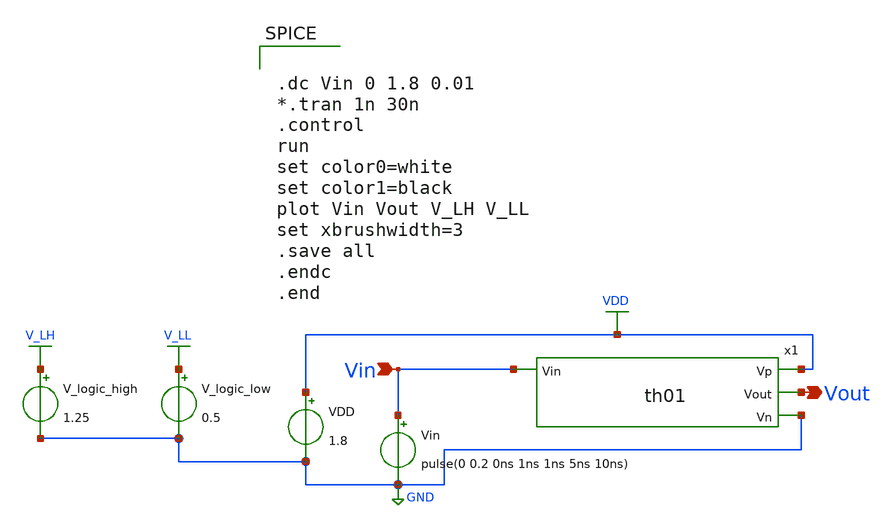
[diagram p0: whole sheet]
** sch_path: xschem/Vth_sch/Pre_layout/th01.sch
**.subckt th01 Vin Vout
*.ipin Vin
*.opin Vout
VDD VDD GND 1.8
Vin Vin GND pulse(0 0.2 0ns 1ns 1ns 5ns 10ns)
V_logic_high V_LH GND 1.25
V_logic_low V_LL GND 0.5
x1 VDD Vin Vout GND th01
**** begin user architecture code


.lib /usr/local/share/pdk/sky130A/libs.tech/ngspice/sky130.lib.spice tt

.save all





.dc Vin 0 1.8 0.01
*.tran 1n 30n
.control
run
set color0=white
set color1=black
plot Vin Vout V_LH V_LL
set xbrushwidth=3
.save all
.endc
.end


**** end user architecture code
**.ends

* expanding   symbol:  Symbol/th01.sym # of pins=4
** sym_path: xschem/Vth_sch/Symbol/th01.sym
** sch_path: xschem/Vth_sch/Symbol/th01.sch
.subckt th01 Vp Vin Vout Vn
*.opin Vn
*.opin Vp
*.ipin Vin
*.opin Vout
XM1 Vn Vin net1 net1 sky130_fd_pr__pfet_01v8 L=1.1 W=0.42 nf=1 ad='int((nf+1)/2) * W/nf * 0.29' as='int((nf+2)/2) * W/nf * 0.29'
+ pd='2*int((nf+1)/2) * (W/nf + 0.29)' ps='2*int((nf+2)/2) * (W/nf + 0.29)' nrd='0.29 / W' nrs='0.29 / W'
+ sa=0 sb=0 sd=0 mult=1 m=1
XM2 Vp Vin net1 net1 sky130_fd_pr__nfet_01v8 L=12 W=0.36 nf=1 ad='int((nf+1)/2) * W/nf * 0.29' as='int((nf+2)/2) * W/nf * 0.29'
+ pd='2*int((nf+1)/2) * (W/nf + 0.29)' ps='2*int((nf+2)/2) * (W/nf + 0.29)' nrd='0.29 / W' nrs='0.29 / W'
+ sa=0 sb=0 sd=0 mult=1 m=1
XM7 Vout net2 Vp Vp sky130_fd_pr__pfet_01v8 L=0.15 W=0.42 nf=1 ad='int((nf+1)/2) * W/nf * 0.29' as='int((nf+2)/2) * W/nf * 0.29'
+ pd='2*int((nf+1)/2) * (W/nf + 0.29)' ps='2*int((nf+2)/2) * (W/nf + 0.29)' nrd='0.29 / W' nrs='0.29 / W'
+ sa=0 sb=0 sd=0 mult=1 m=1
XM10 Vout net2 Vn Vn sky130_fd_pr__nfet_01v8 L=0.22 W=0.42 nf=1 ad='int((nf+1)/2) * W/nf * 0.29' as='int((nf+2)/2) * W/nf * 0.29'
+ pd='2*int((nf+1)/2) * (W/nf + 0.29)' ps='2*int((nf+2)/2) * (W/nf + 0.29)' nrd='0.29 / W' nrs='0.29 / W'
+ sa=0 sb=0 sd=0 mult=1 m=1
XM3 net2 net1 Vp Vp sky130_fd_pr__pfet_01v8 L=0.15 W=0.42 nf=1 ad='int((nf+1)/2) * W/nf * 0.29' as='int((nf+2)/2) * W/nf * 0.29'
+ pd='2*int((nf+1)/2) * (W/nf + 0.29)' ps='2*int((nf+2)/2) * (W/nf + 0.29)' nrd='0.29 / W' nrs='0.29 / W'
+ sa=0 sb=0 sd=0 mult=1 m=1
XM4 net2 net1 Vn Vn sky130_fd_pr__nfet_01v8 L=0.233 W=0.36 nf=1 ad='int((nf+1)/2) * W/nf * 0.29' as='int((nf+2)/2) * W/nf * 0.29'
+ pd='2*int((nf+1)/2) * (W/nf + 0.29)' ps='2*int((nf+2)/2) * (W/nf + 0.29)' nrd='0.29 / W' nrs='0.29 / W'
+ sa=0 sb=0 sd=0 mult=1 m=1
.ends

.GLOBAL VDD
.GLOBAL GND
.GLOBAL V_LH
.GLOBAL V_LL
.end
